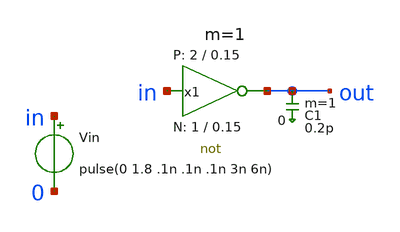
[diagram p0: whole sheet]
** sch_path: xschem/inv_tb.sch
* StefanSchippers/xschem_sky130/sky130_tests/not.sch:
* Copyright 2021 Stefan Frederik Schippers
* Licensed under the Apache License, Version 2.0 (the "License");
**.subckt inv_tb
x1 out in VCC VSS not W_N=1 L_N=0.15 W_P=2 L_P=0.15 m=1
Vin in 0 pulse(0 1.8 .1n .1n .1n 3n 6n)
C1 out 0 0.2p m=1
**** begin user architecture code
 .lib $::SKYWATER_MODELS/sky130.lib.spice tt


vvcc vcc 0 dc 1.8
vvss vss 0 dc 0
.save all alli
.tran 1n 15n
.control
plot in out
.endc


**** end user architecture code
**.ends

* expanding   symbol:  not.sym # of pins=2
** sym_path: not.sym
** sch_path: not.sch
.subckt not y a VCCPIN VSSPIN     W_N=1 L_N=0.15 W_P=2 L_P=0.15
*.opin y
*.ipin a
XM1 DN a VSSPIN VSSPIN sky130_fd_pr__nfet_01v8 L=L_N W=W_N nf=1 ad='int((1 + 1)/2) * W_N / 1 * 0.29'
+ as='int((1 + 2)/2) * W_N / 1 * 0.29' pd='2*int((1 + 1)/2) * (W_N / 1 + 0.29)' ps='2*int((1 + 2)/2) * (W_N / 1 + 0.29)'
+ nrd='0.29 / W_N ' nrs='0.29 / W_N ' sa=0 sb=0 sd=0 mult=1 m=1
XM2 DP a VCCPIN VCCPIN sky130_fd_pr__pfet_01v8 L=L_P W=W_P nf=1 ad='int((nf+1)/2) * W/nf * 0.29' as='int((nf+2)/2) * W/nf * 0.29'
+ pd='2*int((nf+1)/2) * (W/nf + 0.29)' ps='2*int((nf+2)/2) * (W/nf + 0.29)' nrd='0.29 / W' nrs='0.29 / W'
+ sa=0 sb=0 sd=0 mult=1 m=1
Vmeas DP y 0
.save i(vmeas)
Vmeas1 y DN 0
.save i(vmeas1)
.save v(dp)
.save v(dn)
.ends

.end
